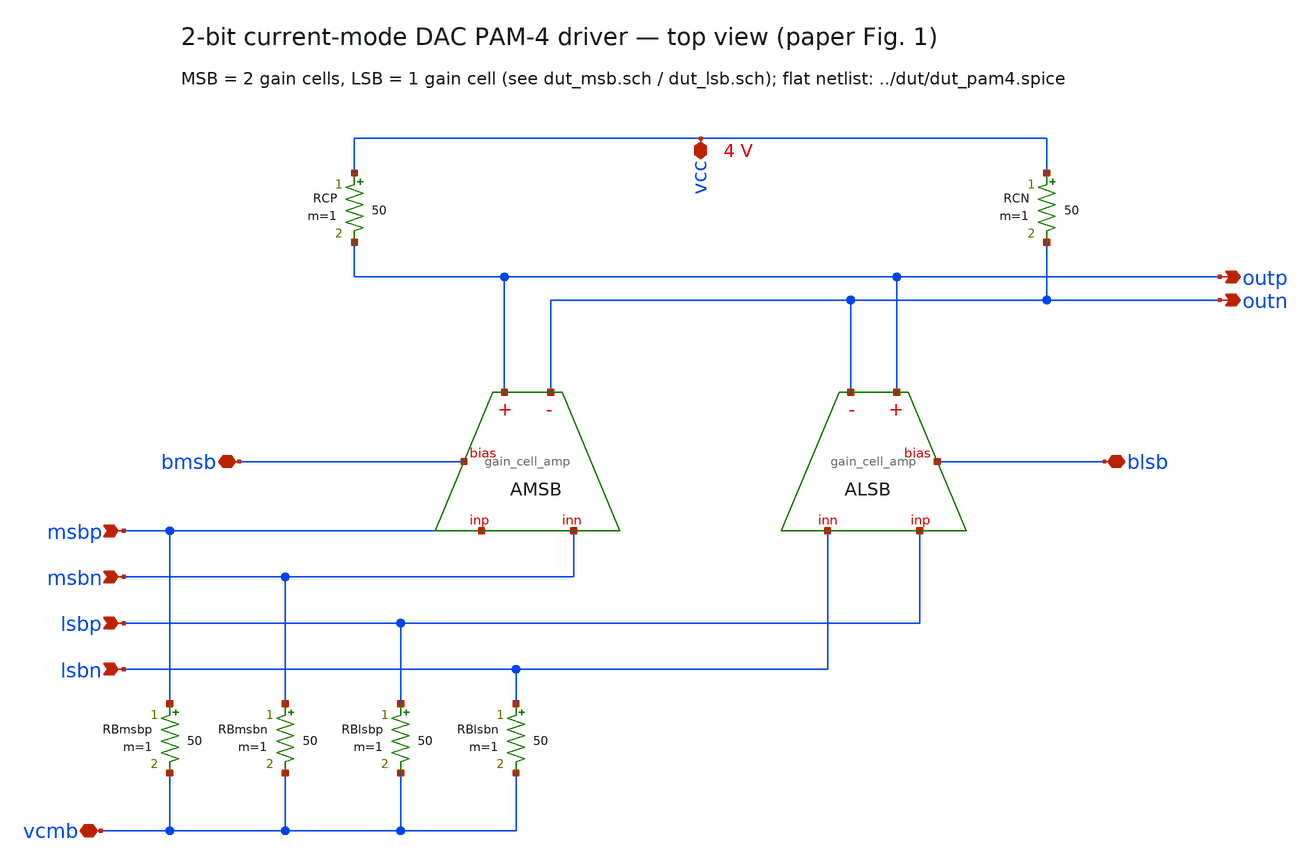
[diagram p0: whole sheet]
** sch_path: analog-db/drawings/pam4-driver-2-bit-dac-HBT/ported-netlists/schematics/dut_pam4.sch
**.subckt dut_pam4 vcc outp outn msbp msbn lsbp lsbn bmsb blsb vcmb
*.iopin vcc
*.opin outp
*.opin outn
*.ipin msbp
*.ipin msbn
*.ipin lsbp
*.ipin lsbn
*.iopin bmsb
*.iopin blsb
*.iopin vcmb
RCP vcc outp 50 m=1
RCN vcc outn 50 m=1
AMSB msbp msbn outp outn bmsb gain_cell_amp
ALSB lsbp lsbn outp outn blsb gain_cell_amp
RBmsbp msbp vcmb 50 m=1
RBmsbn msbn vcmb 50 m=1
RBlsbp lsbp vcmb 50 m=1
RBlsbn lsbn vcmb 50 m=1
**.ends
.end
